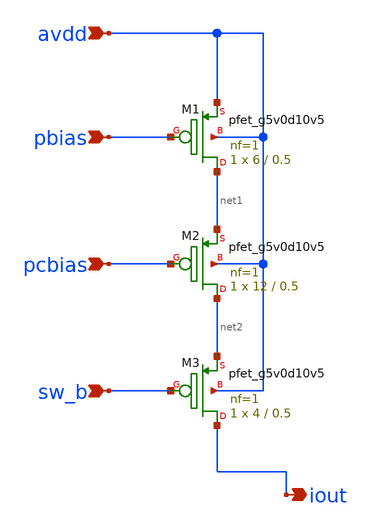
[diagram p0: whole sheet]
** sch_path: xschem/pcell1s.sch
**.subckt pcell1s pbias pcbias sw_b avdd iout
*.ipin pbias
*.ipin pcbias
*.ipin sw_b
*.ipin avdd
*.opin iout
XM1 net1 pbias avdd avdd sky130_fd_pr__pfet_g5v0d10v5 L=0.5 W=6 nf=1 ad='int((nf+1)/2) * W/nf * 0.29'
+ as='int((nf+2)/2) * W/nf * 0.29' pd='2*int((nf+1)/2) * (W/nf + 0.29)' ps='2*int((nf+2)/2) * (W/nf + 0.29)'
+ nrd='0.29 / W' nrs='0.29 / W' sa=0 sb=0 sd=0 mult=1 m=1
XM2 net2 pcbias net1 avdd sky130_fd_pr__pfet_g5v0d10v5 L=0.5 W=12 nf=1 ad='int((nf+1)/2) * W/nf * 0.29'
+ as='int((nf+2)/2) * W/nf * 0.29' pd='2*int((nf+1)/2) * (W/nf + 0.29)' ps='2*int((nf+2)/2) * (W/nf + 0.29)'
+ nrd='0.29 / W' nrs='0.29 / W' sa=0 sb=0 sd=0 mult=1 m=1
XM3 iout sw_b net2 avdd sky130_fd_pr__pfet_g5v0d10v5 L=0.5 W=4 nf=1 ad='int((nf+1)/2) * W/nf * 0.29'
+ as='int((nf+2)/2) * W/nf * 0.29' pd='2*int((nf+1)/2) * (W/nf + 0.29)' ps='2*int((nf+2)/2) * (W/nf + 0.29)'
+ nrd='0.29 / W' nrs='0.29 / W' sa=0 sb=0 sd=0 mult=1 m=1
**.ends
.end
